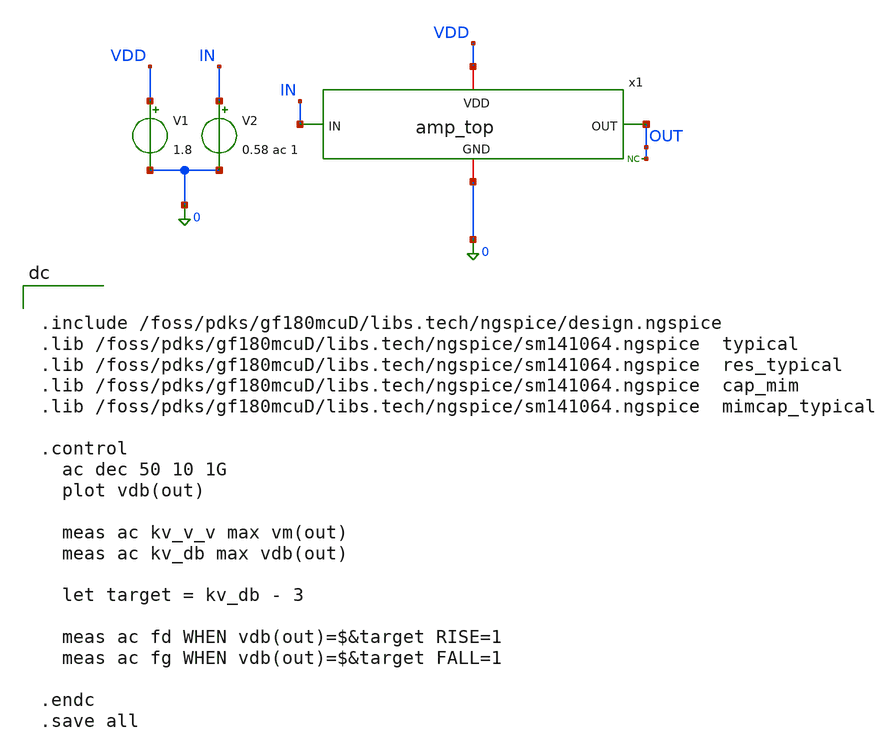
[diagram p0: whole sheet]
** sch_path: amp_top_test.sch
**.subckt amp_top_test
x1 IN OUT VDD 0 amp_top
V1 VDD 0 1.8
V2 IN 0 0.58 ac 1
* noconn OUT
**** begin user architecture code


.include /foss/pdks/gf180mcuD/libs.tech/ngspice/design.ngspice
.lib /foss/pdks/gf180mcuD/libs.tech/ngspice/sm141064.ngspice  typical
.lib /foss/pdks/gf180mcuD/libs.tech/ngspice/sm141064.ngspice  res_typical
.lib /foss/pdks/gf180mcuD/libs.tech/ngspice/sm141064.ngspice  cap_mim
.lib /foss/pdks/gf180mcuD/libs.tech/ngspice/sm141064.ngspice  mimcap_typical

.control
  ac dec 50 10 1G
  plot vdb(out)

  meas ac kv_v_v max vm(out)
  meas ac kv_db max vdb(out)

  let target = kv_db - 3

  meas ac fd WHEN vdb(out)=$&target RISE=1
  meas ac fg WHEN vdb(out)=$&target FALL=1

.endc
.save all


**** end user architecture code
**.ends
.end
